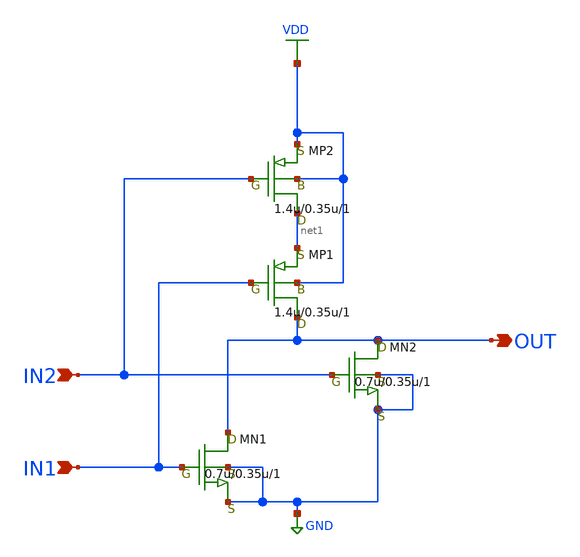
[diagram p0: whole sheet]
** sch_path: LR_hokari/LR_Work2/Clocked_Comparator_Xschem/NOR2.sch
**.subckt NOR2 OUT IN1 IN2
*.opin OUT
*.ipin IN1
*.ipin IN2
MN2 OUT IN2 GND GND nch w=0.7u l=0.35u as=0.56p ps=3u ad=0.56p pd=3u m=1
MP2 net1 IN2 VDD VDD pch w=1.4u l=0.35u as=1.2p ps=4.6u ad=1.2p pd=4.6u m=1
MP1 OUT IN1 net1 VDD pch w=1.4u l=0.35u as=1.2p ps=4.6u ad=1.2p pd=4.6u m=1
MN1 OUT IN1 GND GND nch w=0.7u l=0.35u as=0.56p ps=3u ad=0.56p pd=3u m=1
**.ends
.GLOBAL GND
.GLOBAL VDD
.end
